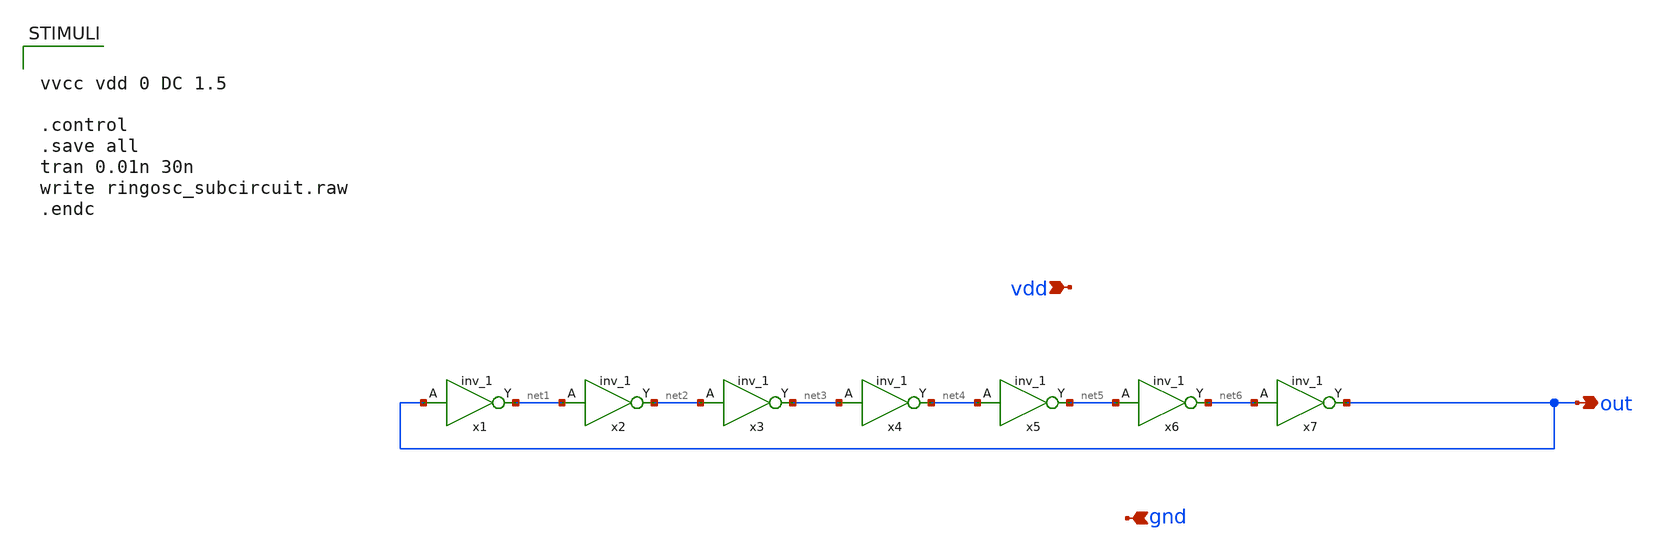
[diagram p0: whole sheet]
** sch_path: images/iic-osic-tools/addons/examples/sky130-analog/designs/ringosc/ringosc_subcircuit.sch
**.subckt ringosc_subcircuit out vdd gnd
*.opin out
*.ipin vdd
*.ipin gnd
x1 out gnd gnd vdd vdd net1 sky130_fd_sc_hd__inv_1
x2 net1 gnd gnd vdd vdd net2 sky130_fd_sc_hd__inv_1
x3 net2 gnd gnd vdd vdd net3 sky130_fd_sc_hd__inv_1
x4 net3 gnd gnd vdd vdd net4 sky130_fd_sc_hd__inv_1
x5 net4 gnd gnd vdd vdd net5 sky130_fd_sc_hd__inv_1
x6 net5 gnd gnd vdd vdd net6 sky130_fd_sc_hd__inv_1
x7 net6 gnd gnd vdd vdd out sky130_fd_sc_hd__inv_1
**** begin user architecture code


vvcc vdd 0 DC 1.5

.control
.save all
tran 0.01n 30n
write ringosc_subcircuit.raw
.endc



.include $::SKYWATER_MODELS/cells/nfet_01v8/sky130_fd_pr__nfet_01v8__tt.corner.spice
.include $::SKYWATER_MODELS/cells/nfet_01v8_lvt/sky130_fd_pr__nfet_01v8_lvt__tt.corner.spice
.include $::SKYWATER_MODELS/cells/pfet_01v8/sky130_fd_pr__pfet_01v8__tt.corner.spice
.include $::SKYWATER_MODELS/cells/nfet_03v3_nvt/sky130_fd_pr__nfet_03v3_nvt__tt.corner.spice
.include $::SKYWATER_MODELS/cells/nfet_05v0_nvt/sky130_fd_pr__nfet_05v0_nvt__tt.corner.spice
.include $::SKYWATER_MODELS/cells/esd_nfet_01v8/sky130_fd_pr__esd_nfet_01v8__tt.corner.spice
.include $::SKYWATER_MODELS/cells/pfet_01v8_lvt/sky130_fd_pr__pfet_01v8_lvt__tt.corner.spice
.include $::SKYWATER_MODELS/cells/pfet_01v8_hvt/sky130_fd_pr__pfet_01v8_hvt__tt.corner.spice
.include $::SKYWATER_MODELS/cells/esd_pfet_g5v0d10v5/sky130_fd_pr__esd_pfet_g5v0d10v5__tt.corner.spice
.include $::SKYWATER_MODELS/cells/pfet_g5v0d10v5/sky130_fd_pr__pfet_g5v0d10v5__tt.corner.spice
.include $::SKYWATER_MODELS/cells/pfet_g5v0d16v0/sky130_fd_pr__pfet_g5v0d16v0__tt.corner.spice
.include $::SKYWATER_MODELS/cells/nfet_g5v0d10v5/sky130_fd_pr__nfet_g5v0d10v5__tt.corner.spice
.include $::SKYWATER_MODELS/cells/nfet_g5v0d16v0/sky130_fd_pr__nfet_g5v0d16v0__tt_discrete.corner.spice
.include $::SKYWATER_MODELS/cells/esd_nfet_g5v0d10v5/sky130_fd_pr__esd_nfet_g5v0d10v5__tt.corner.spice
.include $::SKYWATER_MODELS/models/corners/tt/nonfet.spice
* Mismatch parameters
.include $::SKYWATER_MODELS/cells/nfet_01v8/sky130_fd_pr__nfet_01v8__mismatch.corner.spice
.include $::SKYWATER_MODELS/cells/pfet_01v8/sky130_fd_pr__pfet_01v8__mismatch.corner.spice
.include $::SKYWATER_MODELS/cells/nfet_01v8_lvt/sky130_fd_pr__nfet_01v8_lvt__mismatch.corner.spice
.include $::SKYWATER_MODELS/cells/pfet_01v8_lvt/sky130_fd_pr__pfet_01v8_lvt__mismatch.corner.spice
.include $::SKYWATER_MODELS/cells/pfet_01v8_hvt/sky130_fd_pr__pfet_01v8_hvt__mismatch.corner.spice
.include $::SKYWATER_MODELS/cells/nfet_g5v0d10v5/sky130_fd_pr__nfet_g5v0d10v5__mismatch.corner.spice
.include $::SKYWATER_MODELS/cells/pfet_g5v0d10v5/sky130_fd_pr__pfet_g5v0d10v5__mismatch.corner.spice
.include $::SKYWATER_MODELS/cells/nfet_05v0_nvt/sky130_fd_pr__nfet_05v0_nvt__mismatch.corner.spice
.include $::SKYWATER_MODELS/cells/nfet_03v3_nvt/sky130_fd_pr__nfet_03v3_nvt__mismatch.corner.spice
* Resistor$::SKYWATER_MODELS/Capacitor
.include $::SKYWATER_MODELS/models/r+c/res_typical__cap_typical.spice
.include $::SKYWATER_MODELS/models/r+c/res_typical__cap_typical__lin.spice
* Special cells
.include $::SKYWATER_MODELS/models/corners/tt/specialized_cells.spice
* All models
.include $::SKYWATER_MODELS/models/all.spice
* Corner
.include $::SKYWATER_MODELS/models/corners/tt/rf.spice

**** end user architecture code
**.ends
**** begin user architecture code
[sky130_models]
**** end user architecture code
.end
